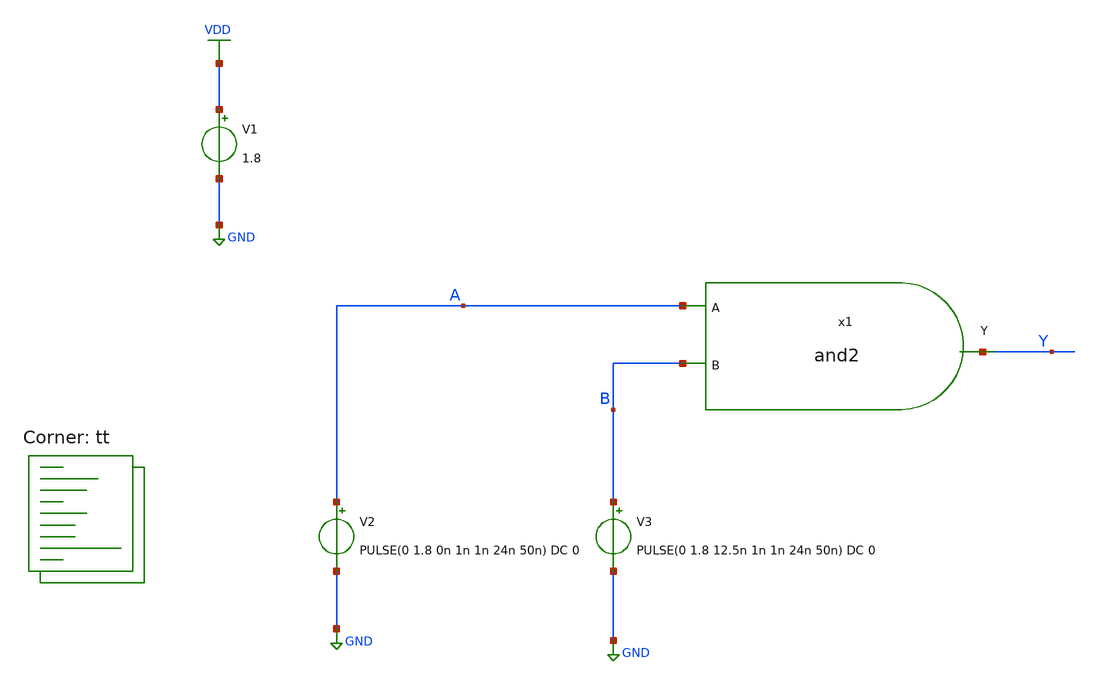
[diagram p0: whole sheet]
** sch_path: eng331lab_final/eng331lab_xschem/tb_and2.sch
**.subckt tb_and2
x1 A Y B and2
V1 VDD GND 1.8
V2 A GND PULSE(0 1.8 0n 1n 1n 24n 50n) DC 0
V3 B GND PULSE(0 1.8 12.5n 1n 1n 24n 50n) DC 0
**** begin user architecture code

.control
  save all
  tran 10n 400n
  write tb_and2.raw
  set appendwrite
.endc


.lib $::SKYWATER_MODELS/sky130.lib.spice tt
**** end user architecture code
**.ends

* expanding   symbol:  eng331lab_xschem/and2.sym # of pins=3
** sym_path: eng331lab_final/eng331lab_xschem/and2.sym
** sch_path: eng331lab_final/eng331lab_xschem/and2.sch
.subckt and2 A Y B
*.ipin A
*.ipin B
*.opin Y
x1e A Y_bar B nand2
x2 Y Y_bar inv
.ends


* expanding   symbol:  eng331_debug/eng331lab_xschem/nand2.sym # of pins=3
** sym_path: eng331lab_final/eng331lab_xschem/nand2.sym
** sch_path: eng331lab_final/eng331lab_xschem/nand2.sch
.subckt nand2 A Y B
*.ipin A
*.ipin B
*.opin Y
XM1 Y A VDD VDD sky130_fd_pr__pfet_01v8 L=0.15 W=0.8 nf=1 ad='int((1 + 1)/2) * 0.8 / 1 * 0.29' as='int((1 + 2)/2) * 0.8 / 1 * 0.29'
+ pd='2*int((1 + 1)/2) * (0.8 / 1 + 0.29)' ps='2*int((1 + 2)/2) * (0.8 / 1 + 0.29)' nrd='0.29 / 0.8 ' nrs='0.29 / 0.8 '
+ sa=0 sb=0 sd=0 mult=1 m=1
XM2 Y B VDD VDD sky130_fd_pr__pfet_01v8 L=0.15 W=0.8 nf=1 ad='int((1 + 1)/2) * 0.8 / 1 * 0.29' as='int((1 + 2)/2) * 0.8 / 1 * 0.29'
+ pd='2*int((1 + 1)/2) * (0.8 / 1 + 0.29)' ps='2*int((1 + 2)/2) * (0.8 / 1 + 0.29)' nrd='0.29 / 0.8 ' nrs='0.29 / 0.8 '
+ sa=0 sb=0 sd=0 mult=1 m=1
XM3 Y A net1 GND sky130_fd_pr__nfet_01v8 L=0.15 W=1 nf=1 ad='int((1 + 1)/2) * 1 / 1 * 0.29' as='int((1 + 2)/2) * 1 / 1 * 0.29'
+ pd='2*int((1 + 1)/2) * (1 / 1 + 0.29)' ps='2*int((1 + 2)/2) * (1 / 1 + 0.29)' nrd='0.29 / 1 ' nrs='0.29 / 1 '
+ sa=0 sb=0 sd=0 mult=1 m=1
XM4 net1 B GND GND sky130_fd_pr__nfet_01v8 L=0.15 W=1 nf=1 ad='int((1 + 1)/2) * 1 / 1 * 0.29' as='int((1 + 2)/2) * 1 / 1 * 0.29'
+ pd='2*int((1 + 1)/2) * (1 / 1 + 0.29)' ps='2*int((1 + 2)/2) * (1 / 1 + 0.29)' nrd='0.29 / 1 ' nrs='0.29 / 1 '
+ sa=0 sb=0 sd=0 mult=1 m=1
.ends


* expanding   symbol:  eng331_debug/eng331lab_xschem/inv.sym # of pins=2
** sym_path: eng331lab_final/eng331lab_xschem/inv.sym
** sch_path: eng331lab_final/eng331lab_xschem/inv.sch
.subckt inv Y A
*.ipin A
*.opin Y
XM1 Y A VDD VDD sky130_fd_pr__pfet_01v8 L=0.15 W=0.8 nf=1 ad='int((1 + 1)/2) * 0.8 / 1 * 0.29' as='int((1 + 2)/2) * 0.8 / 1 * 0.29'
+ pd='2*int((1 + 1)/2) * (0.8 / 1 + 0.29)' ps='2*int((1 + 2)/2) * (0.8 / 1 + 0.29)' nrd='0.29 / 0.8 ' nrs='0.29 / 0.8 '
+ sa=0 sb=0 sd=0 mult=1 m=1
XM2 Y A GND GND sky130_fd_pr__nfet_01v8 L=0.15 W=0.5 nf=1 ad='int((1 + 1)/2) * 0.5 / 1 * 0.29' as='int((1 + 2)/2) * 0.5 / 1 * 0.29'
+ pd='2*int((1 + 1)/2) * (0.5 / 1 + 0.29)' ps='2*int((1 + 2)/2) * (0.5 / 1 + 0.29)' nrd='0.29 / 0.5 ' nrs='0.29 / 0.5 '
+ sa=0 sb=0 sd=0 mult=1 m=1
.ends

.GLOBAL VDD
.GLOBAL GND
.end
